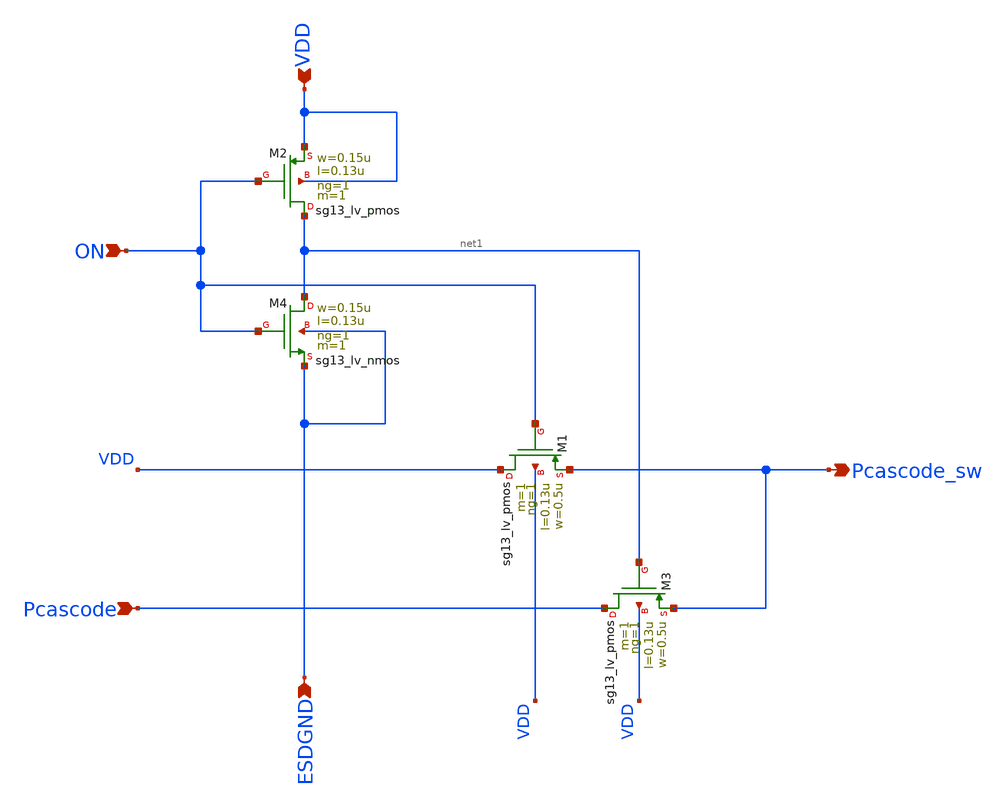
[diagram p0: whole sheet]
** sch_path: schematic/DAC_SW.sch
**.subckt DAC_SW ON Pcascode ESDGND VDD Pcascode_sw
*.ipin ON
*.ipin Pcascode
*.ipin ESDGND
*.ipin VDD
*.opin Pcascode_sw
XM1 VDD ON Pcascode_sw VDD sg13_lv_pmos w=0.5u l=0.13u ng=1 m=1 mm_ok=1
XM2 net1 ON VDD VDD sg13_lv_pmos w=0.15u l=0.13u ng=1 m=1 mm_ok=1
XM3 Pcascode net1 Pcascode_sw VDD sg13_lv_pmos w=0.5u l=0.13u ng=1 m=1 mm_ok=1
XM4 net1 ON ESDGND ESDGND sg13_lv_nmos w=0.15u l=0.13u ng=1 m=1 mm_ok=1
**.ends
.end
